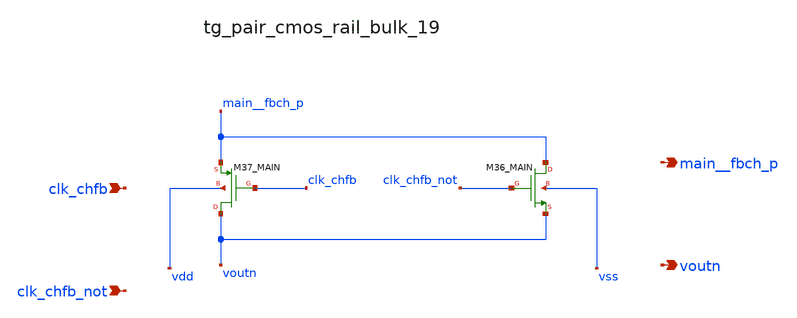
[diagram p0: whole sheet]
** sch_path: analog-db/raw/ia_004_fan_chopper_rrl/hier/blocks/tg_pair_cmos_rail_bulk_19.sch
**.subckt tg_pair_cmos_rail_bulk_19 clk_chfb clk_chfb_not main__fbch_p voutn
*.ipin clk_chfb
*.ipin clk_chfb_not
*.opin main__fbch_p
*.opin voutn
XM36_MAIN main__fbch_p clk_chfb_not voutn vss sg13_lv_nmos w=x_dut_xm36_main_w l=x_dut_xm36_main_l
+ ng=1 m=x_dut_xm36_main_m
XM37_MAIN voutn clk_chfb main__fbch_p vdd sg13_lv_pmos w=x_dut_xm37_main_w l=x_dut_xm37_main_l ng=1
+ m=x_dut_xm37_main_m
**.ends
.end
